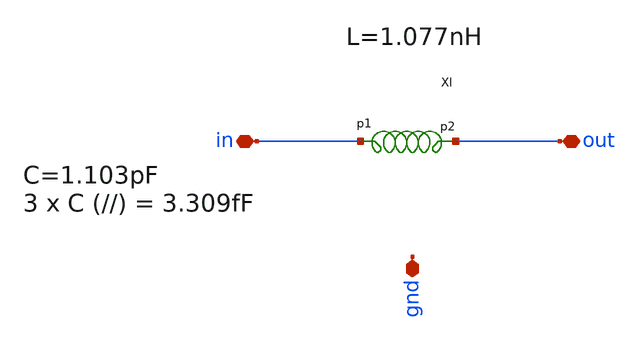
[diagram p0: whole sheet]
** sch_path: impedance-transformer/xschem/impedance-transformer-pex.sch
**.subckt impedance-transformer-pex gnd in out
*.iopin gnd
*.iopin in
*.iopin out
xl1 in out l1
**** begin user architecture code

* NGSPICE file created from impedance-transformer.ext - technology: sky130A

.subckt sky130_fd_pr__cap_mim_m3_2_EJYTBJ c2_n2743_n8292# m4_n2843_n8392# VSUBS
X0 c2_n2743_n8292# m4_n2843_n8392# sky130_fd_pr__cap_mim_m3_2 l=2.664e+07u w=2.664e+07u
X1 c2_n2743_n8292# m4_n2843_n8392# sky130_fd_pr__cap_mim_m3_2 l=2.664e+07u w=2.664e+07u
X2 c2_n2743_n8292# m4_n2843_n8392# sky130_fd_pr__cap_mim_m3_2 l=2.664e+07u w=2.664e+07u
C0 c2_n2743_n8292# m4_n2843_n8392# 139.05fF
C1 c2_n2743_n8292# VSUBS 0.26fF
C2 m4_n2843_n8392# VSUBS 34.85fF
.ends

.subckt sky130_fd_pr__cap_mim_m3_2_5MQ5FR c2_n2229_n6750# m4_n2329_n6850# VSUBS
X0 c2_n2229_n6750# m4_n2329_n6850# sky130_fd_pr__cap_mim_m3_2 l=2.15e+07u w=2.15e+07u
X1 c2_n2229_n6750# m4_n2329_n6850# sky130_fd_pr__cap_mim_m3_2 l=2.15e+07u w=2.15e+07u
X2 c2_n2229_n6750# m4_n2329_n6850# sky130_fd_pr__cap_mim_m3_2 l=2.15e+07u w=2.15e+07u
C0 c2_n2229_n6750# m4_n2329_n6850# 98.38fF
C1 c2_n2229_n6750# VSUBS 0.26fF
C2 m4_n2329_n6850# VSUBS 25.68fF
.ends

*.subckt impedance-transformer gnd in out
Xsky130_fd_pr__cap_mim_m3_2_EJYTBJ_0 out gnd gnd sky130_fd_pr__cap_mim_m3_2_EJYTBJ
Xsky130_fd_pr__cap_mim_m3_2_5MQ5FR_0 in gnd gnd sky130_fd_pr__cap_mim_m3_2_5MQ5FR
Xsky130_fd_pr__cap_mim_m3_2_EJYTBJ_1 out gnd gnd sky130_fd_pr__cap_mim_m3_2_EJYTBJ
Xsky130_fd_pr__cap_mim_m3_2_5MQ5FR_1 in gnd gnd sky130_fd_pr__cap_mim_m3_2_5MQ5FR
Xsky130_fd_pr__cap_mim_m3_2_EJYTBJ_2 out gnd gnd sky130_fd_pr__cap_mim_m3_2_EJYTBJ
Xsky130_fd_pr__cap_mim_m3_2_5MQ5FR_2 in gnd gnd sky130_fd_pr__cap_mim_m3_2_5MQ5FR
Xsky130_fd_pr__cap_mim_m3_2_EJYTBJ_3 out gnd gnd sky130_fd_pr__cap_mim_m3_2_EJYTBJ

R0 out.n0 out.t2 0.196
R1 out.n1 out.n0 0.127
R2 out.n2 out.n1 0.126
R3 out out.n2 0.08
R4 out.n2 out.t11 0.069
R5 out.n0 out.t5 0.068
R6 out.n1 out.t8 0.068
R7 out.t1 out.t0 0.066
R8 out.t2 out.t1 0.066
R9 out.t4 out.t3 0.066
R10 out.t5 out.t4 0.066
R11 out.t7 out.t6 0.066
R12 out.t8 out.t7 0.066
R13 out.t10 out.t9 0.066
R14 out.t11 out.t10 0.066
R15 in in.n1 0.21
R16 in.n0 in.t7 0.137
R17 in.n1 in.n0 0.089
R18 in.n1 in.t1 0.067
R19 in.n0 in.t4 0.067
R20 in.t0 in.t2 0.066
R21 in.t1 in.t0 0.066
R22 in.t3 in.t5 0.066
R23 in.t4 in.t3 0.066
R24 in.t6 in.t8 0.066
R25 in.t7 in.t6 0.066
C0 in out 26.83fF
C1 in.t2 gnd 24.39fF
C2 in.t0 gnd 24.47fF
C3 in.t1 gnd 24.60fF
C4 in.t5 gnd 24.39fF
C5 in.t3 gnd 24.47fF
C6 in.t4 gnd 24.60fF
C7 in.t8 gnd 24.39fF
C8 in.t6 gnd 24.47fF
C9 in.t7 gnd 130.87fF
C10 in.n0 gnd 91.09fF $ **FLOATING
C11 in.n1 gnd 13.77fF $ **FLOATING
C12 out.t9 gnd 45.96fF
C13 out.t10 gnd 46.05fF
C14 out.t11 gnd 45.61fF
C15 out.t6 gnd 45.96fF
C16 out.t7 gnd 46.05fF
C17 out.t8 gnd 45.49fF
C18 out.t3 gnd 45.96fF
C19 out.t4 gnd 46.05fF
C20 out.t5 gnd 45.49fF
C21 out.t0 gnd 45.96fF
C22 out.t1 gnd 46.05fF
C23 out.t2 gnd 50.36fF
C24 out.n0 gnd 14.91fF $ **FLOATING
C25 out.n1 gnd 24.47fF $ **FLOATING
C26 out.n2 gnd 14.19fF $ **FLOATING
C27 in gnd 112.74fF
C28 out gnd 27.16fF
*.ends



**** end user architecture code
**.ends

* expanding   symbol:  /home/hugodg/projects_sky130/temp_sensor/impedance-transformer/xschem/l1.sym
*+ # of pins=2
** sym_path: impedance-transformer/xschem/l1.sym
** sch_path: impedance-transformer/xschem/l1.sch
.subckt l1 p1 p2
*.iopin p2
*.iopin p1
L0 p1 net3 694.6p m=1
Cs1 p1 net1 15.23f m=1
Cs2 p2 net2 16.88f m=1
Rs1 net1 GND 88.99 m=1
Rs2 net2 GND -52.45 m=1
R1 p2 net3 2.899 m=1
.ends

.GLOBAL GND
.end
